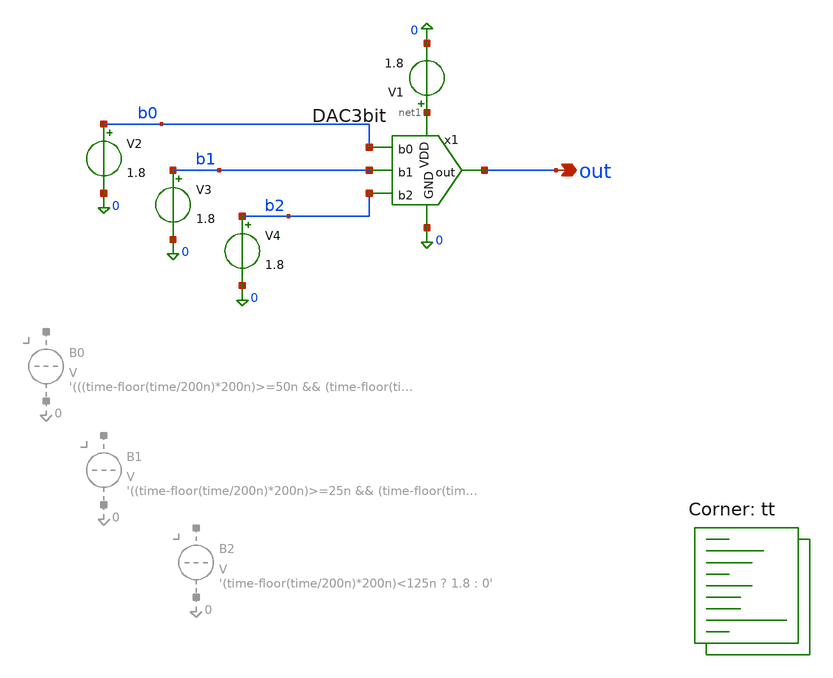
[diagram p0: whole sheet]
** sch_path: xschem/DAC3bit_tb.sch
**.subckt DAC3bit_tb out
*.opin out
x1 b0 b1 b2 net1 out 0 DAC3bit
V1 net1 0 1.8
V2 b0 0 1.8
V3 b1 0 1.8
V4 b2 0 1.8
**** begin user architecture code
.lib $::SKYWATER_MODELS/sky130.lib.spice tt


.control
save all

let n_codes = 8
let vout_meas = unitvec(n_codes)
let code = 0
let bit0 = 0
let bit1 = 0
let bit2 = 0
dowhile bit2 < 2
  dowhile bit1 < 2
    dowhile bit0 < 2
      alter V2 = bit0 * 1.8
      alter V3 = bit1 * 1.8
      alter V4 = bit2 * 1.8
      op
      let vout_value=v(out)
      let vout_meas[code]=vout_value
      echo Codice $&code : b2=$&bit2 b1=$&bit1 b0=$&bit0, Vout=$&vout_value V
      let bit0 = bit0 + 1
      let code = code + 1
    end
    let bit1 = bit1 + 1
    let bit0 = 0
  end
  let bit2 = bit2 + 1
  let bit1 = 0
end
let v_min = vout_meas[0]
let v_max = vout_meas[n_codes - 1]
let lsb_ideal = (v_max - v_min) / (n_codes - 1)
echo ======================================
echo LSB ideale = $&lsb_ideal V
let dnl = unitvec(n_codes)
let i = 1
dowhile i < n_codes
  let step_reale = vout_meas[i] - vout_meas[i-1]
  let dnl[i] = (step_reale / lsb_ideal) - 1
  let dnl_curr = dnl[i]
  echo DNL codice $&i : $&dnl_curr LSB
  let i = i + 1
end
let inl = unitvec(n_codes)
let l = 0
dowhile l < n_codes
  let v_ideal = v_min + l * lsb_ideal
  let inl[l] = (vout_meas[l] - v_ideal) / lsb_ideal
  let inl_curr = inl[l]
  echo INL codice $&l : $&inl_curr LSB
  let l = l + 1
end
echo ======================================
echo Vout min/max: $&v_min V / $&v_max V
echo ======================================
print vout_meas > dac_transfer.txt
print dnl > dac_dnl.txt
print inl > dac_inl.txt
write DAC3bit_op.raw
ac dec 20 1k 100meg
write DAC3bit_ac.raw
tran 1n 5u
write DAC3bit_tran.raw
.endc

**** end user architecture code
**.ends

* expanding   symbol:  DAC3bit.sym # of pins=6
** sym_path: xschem/DAC3bit.sym
** sch_path: xschem/DAC3bit.sch
.subckt DAC3bit b0 b1 b2 VDD out GND
*.opin out
*.ipin b0
*.ipin b1
*.ipin b2
*.ipin GND
*.ipin VDD
XR1 GND net3 sky130_fd_pr__res_generic_po W=1 L=21 m=1
XR2 net3 net1 sky130_fd_pr__res_generic_po W=1 L=21 m=1
XR3 b0 net4 sky130_fd_pr__res_generic_po W=1 L=21 m=1
XR4 net4 net1 sky130_fd_pr__res_generic_po W=1 L=21 m=1
XR5 b1 net5 sky130_fd_pr__res_generic_po W=1 L=21 m=1
XR6 net5 net2 sky130_fd_pr__res_generic_po W=1 L=21 m=1
XR7 b2 net6 sky130_fd_pr__res_generic_po W=1 L=21 m=1
XR8 net6 vx sky130_fd_pr__res_generic_po W=1 L=21 m=1
XR9 net1 net2 sky130_fd_pr__res_generic_po W=1 L=21 m=1
XR10 net2 vx sky130_fd_pr__res_generic_po W=1 L=21 m=1
XR12 VDD out sky130_fd_pr__res_generic_po W=1 L=21 m=1
XR13 out GND sky130_fd_pr__res_generic_po W=1 L=21 m=1
XR11 out vx sky130_fd_pr__res_generic_po W=1 L=63 m=1
.ends

.end
